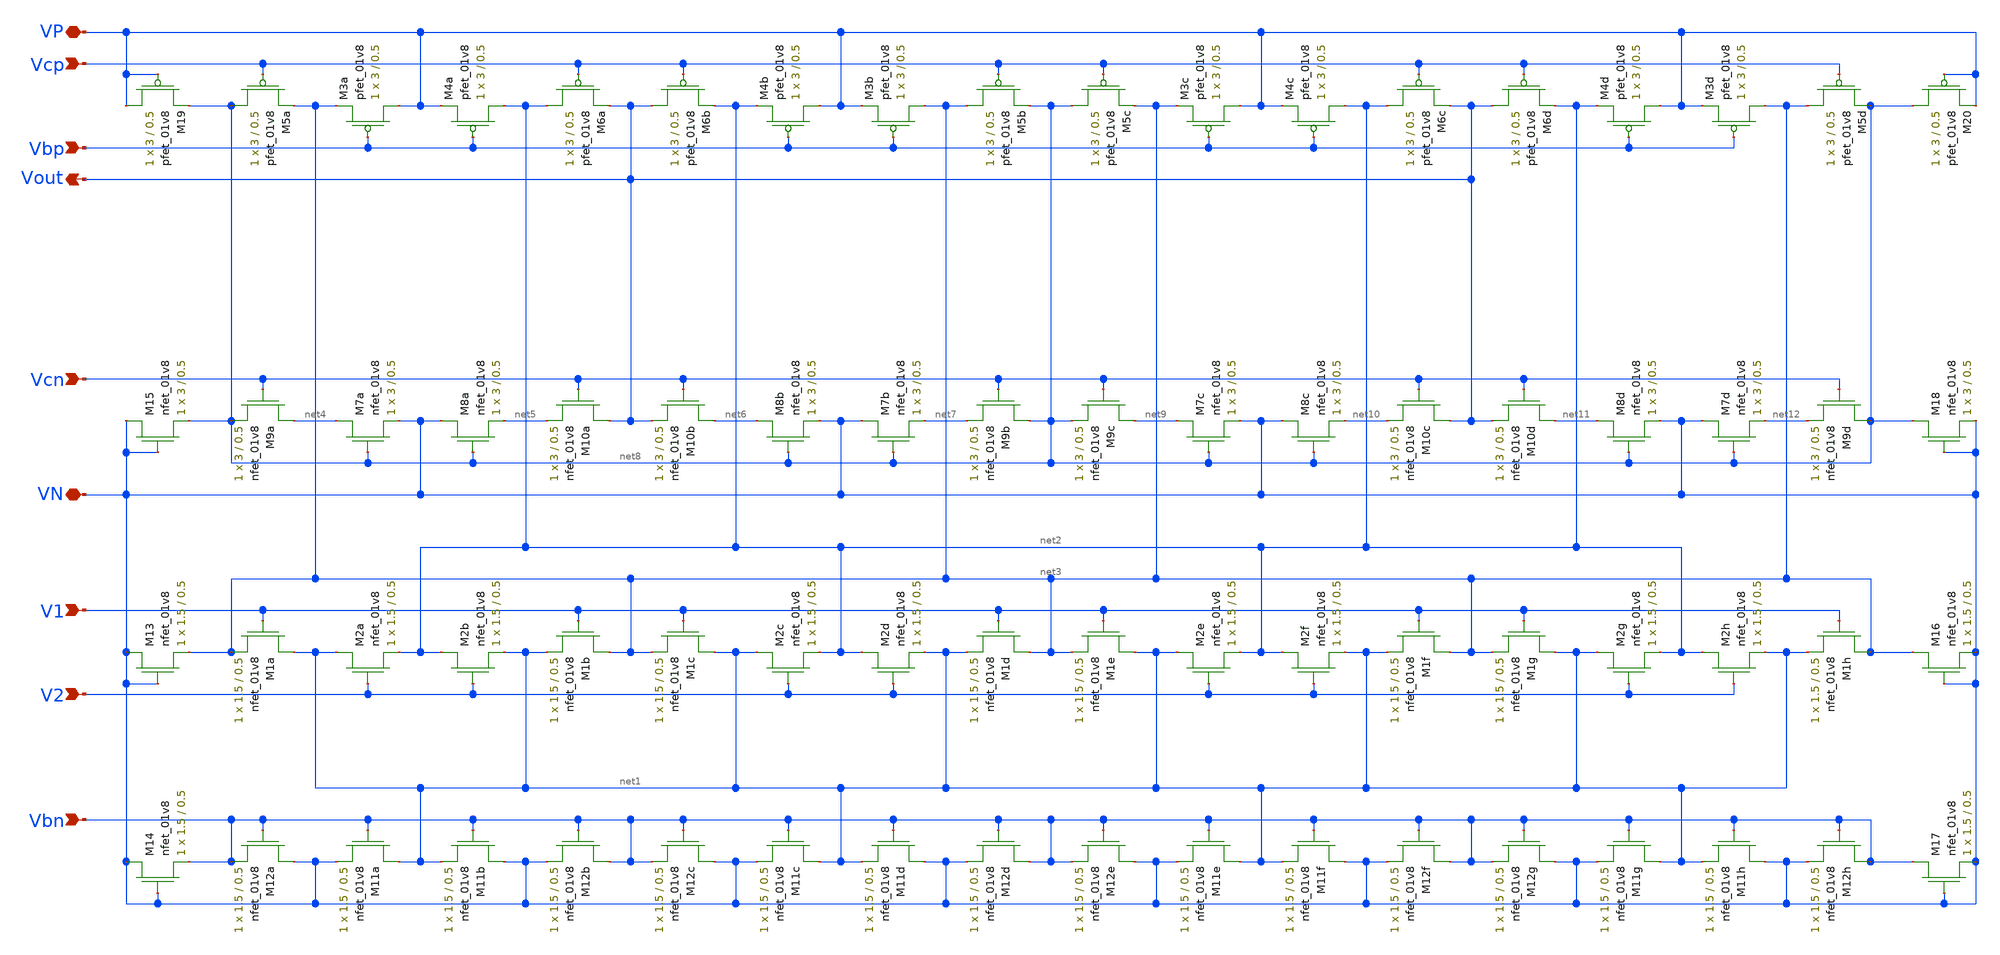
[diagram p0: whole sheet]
** sch_path: fc_diffamp_lds.sch
**.subckt fc_diffamp_lds V1 V2 Vout VN VP Vcp Vbp Vcn Vbn
*.ipin V1
*.ipin V2
*.opin Vout
*.iopin VN
*.iopin VP
*.ipin Vcp
*.ipin Vbp
*.ipin Vcn
*.ipin Vbn
XM1a net1 V1 net3 GND sky130_fd_pr__nfet_01v8 L=0.5 W=1.5 nf=1 ad='int((nf+1)/2) * W/nf * 0.29' as='int((nf+2)/2) * W/nf * 0.29'
+ pd='2*int((nf+1)/2) * (W/nf + 0.29)' ps='2*int((nf+2)/2) * (W/nf + 0.29)' nrd='0.29 / W' nrs='0.29 / W'
+ sa=0 sb=0 sd=0 mult=1 m=1
XM2a net1 V2 net2 GND sky130_fd_pr__nfet_01v8 L=0.5 W=1.5 nf=1 ad='int((nf+1)/2) * W/nf * 0.29' as='int((nf+2)/2) * W/nf * 0.29'
+ pd='2*int((nf+1)/2) * (W/nf + 0.29)' ps='2*int((nf+2)/2) * (W/nf + 0.29)' nrd='0.29 / W' nrs='0.29 / W'
+ sa=0 sb=0 sd=0 mult=1 m=1
XM2b net2 V2 net1 GND sky130_fd_pr__nfet_01v8 L=0.5 W=1.5 nf=1 ad='int((nf+1)/2) * W/nf * 0.29' as='int((nf+2)/2) * W/nf * 0.29'
+ pd='2*int((nf+1)/2) * (W/nf + 0.29)' ps='2*int((nf+2)/2) * (W/nf + 0.29)' nrd='0.29 / W' nrs='0.29 / W'
+ sa=0 sb=0 sd=0 mult=1 m=1
XM1b net3 V1 net1 GND sky130_fd_pr__nfet_01v8 L=0.5 W=1.5 nf=1 ad='int((nf+1)/2) * W/nf * 0.29' as='int((nf+2)/2) * W/nf * 0.29'
+ pd='2*int((nf+1)/2) * (W/nf + 0.29)' ps='2*int((nf+2)/2) * (W/nf + 0.29)' nrd='0.29 / W' nrs='0.29 / W'
+ sa=0 sb=0 sd=0 mult=1 m=1
XM1c net1 V1 net3 GND sky130_fd_pr__nfet_01v8 L=0.5 W=1.5 nf=1 ad='int((nf+1)/2) * W/nf * 0.29' as='int((nf+2)/2) * W/nf * 0.29'
+ pd='2*int((nf+1)/2) * (W/nf + 0.29)' ps='2*int((nf+2)/2) * (W/nf + 0.29)' nrd='0.29 / W' nrs='0.29 / W'
+ sa=0 sb=0 sd=0 mult=1 m=1
XM2c net1 V2 net2 GND sky130_fd_pr__nfet_01v8 L=0.5 W=1.5 nf=1 ad='int((nf+1)/2) * W/nf * 0.29' as='int((nf+2)/2) * W/nf * 0.29'
+ pd='2*int((nf+1)/2) * (W/nf + 0.29)' ps='2*int((nf+2)/2) * (W/nf + 0.29)' nrd='0.29 / W' nrs='0.29 / W'
+ sa=0 sb=0 sd=0 mult=1 m=1
XM2d net2 V2 net1 GND sky130_fd_pr__nfet_01v8 L=0.5 W=1.5 nf=1 ad='int((nf+1)/2) * W/nf * 0.29' as='int((nf+2)/2) * W/nf * 0.29'
+ pd='2*int((nf+1)/2) * (W/nf + 0.29)' ps='2*int((nf+2)/2) * (W/nf + 0.29)' nrd='0.29 / W' nrs='0.29 / W'
+ sa=0 sb=0 sd=0 mult=1 m=1
XM1d net3 V1 net1 GND sky130_fd_pr__nfet_01v8 L=0.5 W=1.5 nf=1 ad='int((nf+1)/2) * W/nf * 0.29' as='int((nf+2)/2) * W/nf * 0.29'
+ pd='2*int((nf+1)/2) * (W/nf + 0.29)' ps='2*int((nf+2)/2) * (W/nf + 0.29)' nrd='0.29 / W' nrs='0.29 / W'
+ sa=0 sb=0 sd=0 mult=1 m=1
XM11a net1 Vbn VN GND sky130_fd_pr__nfet_01v8 L=0.5 W=1.5 nf=1 ad='int((nf+1)/2) * W/nf * 0.29' as='int((nf+2)/2) * W/nf * 0.29'
+ pd='2*int((nf+1)/2) * (W/nf + 0.29)' ps='2*int((nf+2)/2) * (W/nf + 0.29)' nrd='0.29 / W' nrs='0.29 / W'
+ sa=0 sb=0 sd=0 mult=1 m=1
XM12a VN Vbn Vbn GND sky130_fd_pr__nfet_01v8 L=0.5 W=1.5 nf=1 ad='int((nf+1)/2) * W/nf * 0.29' as='int((nf+2)/2) * W/nf * 0.29'
+ pd='2*int((nf+1)/2) * (W/nf + 0.29)' ps='2*int((nf+2)/2) * (W/nf + 0.29)' nrd='0.29 / W' nrs='0.29 / W'
+ sa=0 sb=0 sd=0 mult=1 m=1
XM12b Vbn Vbn VN GND sky130_fd_pr__nfet_01v8 L=0.5 W=1.5 nf=1 ad='int((nf+1)/2) * W/nf * 0.29' as='int((nf+2)/2) * W/nf * 0.29'
+ pd='2*int((nf+1)/2) * (W/nf + 0.29)' ps='2*int((nf+2)/2) * (W/nf + 0.29)' nrd='0.29 / W' nrs='0.29 / W'
+ sa=0 sb=0 sd=0 mult=1 m=1
XM11b VN Vbn net1 GND sky130_fd_pr__nfet_01v8 L=0.5 W=1.5 nf=1 ad='int((nf+1)/2) * W/nf * 0.29' as='int((nf+2)/2) * W/nf * 0.29'
+ pd='2*int((nf+1)/2) * (W/nf + 0.29)' ps='2*int((nf+2)/2) * (W/nf + 0.29)' nrd='0.29 / W' nrs='0.29 / W'
+ sa=0 sb=0 sd=0 mult=1 m=1
XM11c net1 Vbn VN GND sky130_fd_pr__nfet_01v8 L=0.5 W=1.5 nf=1 ad='int((nf+1)/2) * W/nf * 0.29' as='int((nf+2)/2) * W/nf * 0.29'
+ pd='2*int((nf+1)/2) * (W/nf + 0.29)' ps='2*int((nf+2)/2) * (W/nf + 0.29)' nrd='0.29 / W' nrs='0.29 / W'
+ sa=0 sb=0 sd=0 mult=1 m=1
XM12c VN Vbn Vbn GND sky130_fd_pr__nfet_01v8 L=0.5 W=1.5 nf=1 ad='int((nf+1)/2) * W/nf * 0.29' as='int((nf+2)/2) * W/nf * 0.29'
+ pd='2*int((nf+1)/2) * (W/nf + 0.29)' ps='2*int((nf+2)/2) * (W/nf + 0.29)' nrd='0.29 / W' nrs='0.29 / W'
+ sa=0 sb=0 sd=0 mult=1 m=1
XM12d Vbn Vbn VN GND sky130_fd_pr__nfet_01v8 L=0.5 W=1.5 nf=1 ad='int((nf+1)/2) * W/nf * 0.29' as='int((nf+2)/2) * W/nf * 0.29'
+ pd='2*int((nf+1)/2) * (W/nf + 0.29)' ps='2*int((nf+2)/2) * (W/nf + 0.29)' nrd='0.29 / W' nrs='0.29 / W'
+ sa=0 sb=0 sd=0 mult=1 m=1
XM11d VN Vbn net1 GND sky130_fd_pr__nfet_01v8 L=0.5 W=1.5 nf=1 ad='int((nf+1)/2) * W/nf * 0.29' as='int((nf+2)/2) * W/nf * 0.29'
+ pd='2*int((nf+1)/2) * (W/nf + 0.29)' ps='2*int((nf+2)/2) * (W/nf + 0.29)' nrd='0.29 / W' nrs='0.29 / W'
+ sa=0 sb=0 sd=0 mult=1 m=1
XM9a net4 Vcn net8 GND sky130_fd_pr__nfet_01v8 L=0.5 W=3 nf=1 ad='int((nf+1)/2) * W/nf * 0.29' as='int((nf+2)/2) * W/nf * 0.29'
+ pd='2*int((nf+1)/2) * (W/nf + 0.29)' ps='2*int((nf+2)/2) * (W/nf + 0.29)' nrd='0.29 / W' nrs='0.29 / W'
+ sa=0 sb=0 sd=0 mult=1 m=1
XM7a net4 net8 VN GND sky130_fd_pr__nfet_01v8 L=0.5 W=3 nf=1 ad='int((nf+1)/2) * W/nf * 0.29' as='int((nf+2)/2) * W/nf * 0.29'
+ pd='2*int((nf+1)/2) * (W/nf + 0.29)' ps='2*int((nf+2)/2) * (W/nf + 0.29)' nrd='0.29 / W' nrs='0.29 / W'
+ sa=0 sb=0 sd=0 mult=1 m=1
XM8a VN net8 net5 GND sky130_fd_pr__nfet_01v8 L=0.5 W=3 nf=1 ad='int((nf+1)/2) * W/nf * 0.29' as='int((nf+2)/2) * W/nf * 0.29'
+ pd='2*int((nf+1)/2) * (W/nf + 0.29)' ps='2*int((nf+2)/2) * (W/nf + 0.29)' nrd='0.29 / W' nrs='0.29 / W'
+ sa=0 sb=0 sd=0 mult=1 m=1
XM10a Vout Vcn net5 GND sky130_fd_pr__nfet_01v8 L=0.5 W=3 nf=1 ad='int((nf+1)/2) * W/nf * 0.29' as='int((nf+2)/2) * W/nf * 0.29'
+ pd='2*int((nf+1)/2) * (W/nf + 0.29)' ps='2*int((nf+2)/2) * (W/nf + 0.29)' nrd='0.29 / W' nrs='0.29 / W'
+ sa=0 sb=0 sd=0 mult=1 m=1
XM10b net6 Vcn Vout GND sky130_fd_pr__nfet_01v8 L=0.5 W=3 nf=1 ad='int((nf+1)/2) * W/nf * 0.29' as='int((nf+2)/2) * W/nf * 0.29'
+ pd='2*int((nf+1)/2) * (W/nf + 0.29)' ps='2*int((nf+2)/2) * (W/nf + 0.29)' nrd='0.29 / W' nrs='0.29 / W'
+ sa=0 sb=0 sd=0 mult=1 m=1
XM9b net8 Vcn net7 GND sky130_fd_pr__nfet_01v8 L=0.5 W=3 nf=1 ad='int((nf+1)/2) * W/nf * 0.29' as='int((nf+2)/2) * W/nf * 0.29'
+ pd='2*int((nf+1)/2) * (W/nf + 0.29)' ps='2*int((nf+2)/2) * (W/nf + 0.29)' nrd='0.29 / W' nrs='0.29 / W'
+ sa=0 sb=0 sd=0 mult=1 m=1
XM7b VN net8 net7 GND sky130_fd_pr__nfet_01v8 L=0.5 W=3 nf=1 ad='int((nf+1)/2) * W/nf * 0.29' as='int((nf+2)/2) * W/nf * 0.29'
+ pd='2*int((nf+1)/2) * (W/nf + 0.29)' ps='2*int((nf+2)/2) * (W/nf + 0.29)' nrd='0.29 / W' nrs='0.29 / W'
+ sa=0 sb=0 sd=0 mult=1 m=1
XM8b net6 net8 VN GND sky130_fd_pr__nfet_01v8 L=0.5 W=3 nf=1 ad='int((nf+1)/2) * W/nf * 0.29' as='int((nf+2)/2) * W/nf * 0.29'
+ pd='2*int((nf+1)/2) * (W/nf + 0.29)' ps='2*int((nf+2)/2) * (W/nf + 0.29)' nrd='0.29 / W' nrs='0.29 / W'
+ sa=0 sb=0 sd=0 mult=1 m=1
XM9c net9 Vcn net8 GND sky130_fd_pr__nfet_01v8 L=0.5 W=3 nf=1 ad='int((nf+1)/2) * W/nf * 0.29' as='int((nf+2)/2) * W/nf * 0.29'
+ pd='2*int((nf+1)/2) * (W/nf + 0.29)' ps='2*int((nf+2)/2) * (W/nf + 0.29)' nrd='0.29 / W' nrs='0.29 / W'
+ sa=0 sb=0 sd=0 mult=1 m=1
XM7c net9 net8 VN GND sky130_fd_pr__nfet_01v8 L=0.5 W=3 nf=1 ad='int((nf+1)/2) * W/nf * 0.29' as='int((nf+2)/2) * W/nf * 0.29'
+ pd='2*int((nf+1)/2) * (W/nf + 0.29)' ps='2*int((nf+2)/2) * (W/nf + 0.29)' nrd='0.29 / W' nrs='0.29 / W'
+ sa=0 sb=0 sd=0 mult=1 m=1
XM8c VN net8 net10 GND sky130_fd_pr__nfet_01v8 L=0.5 W=3 nf=1 ad='int((nf+1)/2) * W/nf * 0.29' as='int((nf+2)/2) * W/nf * 0.29'
+ pd='2*int((nf+1)/2) * (W/nf + 0.29)' ps='2*int((nf+2)/2) * (W/nf + 0.29)' nrd='0.29 / W' nrs='0.29 / W'
+ sa=0 sb=0 sd=0 mult=1 m=1
XM10c Vout Vcn net10 GND sky130_fd_pr__nfet_01v8 L=0.5 W=3 nf=1 ad='int((nf+1)/2) * W/nf * 0.29' as='int((nf+2)/2) * W/nf * 0.29'
+ pd='2*int((nf+1)/2) * (W/nf + 0.29)' ps='2*int((nf+2)/2) * (W/nf + 0.29)' nrd='0.29 / W' nrs='0.29 / W'
+ sa=0 sb=0 sd=0 mult=1 m=1
XM10d net11 Vcn Vout GND sky130_fd_pr__nfet_01v8 L=0.5 W=3 nf=1 ad='int((nf+1)/2) * W/nf * 0.29' as='int((nf+2)/2) * W/nf * 0.29'
+ pd='2*int((nf+1)/2) * (W/nf + 0.29)' ps='2*int((nf+2)/2) * (W/nf + 0.29)' nrd='0.29 / W' nrs='0.29 / W'
+ sa=0 sb=0 sd=0 mult=1 m=1
XM9d net8 Vcn net12 GND sky130_fd_pr__nfet_01v8 L=0.5 W=3 nf=1 ad='int((nf+1)/2) * W/nf * 0.29' as='int((nf+2)/2) * W/nf * 0.29'
+ pd='2*int((nf+1)/2) * (W/nf + 0.29)' ps='2*int((nf+2)/2) * (W/nf + 0.29)' nrd='0.29 / W' nrs='0.29 / W'
+ sa=0 sb=0 sd=0 mult=1 m=1
XM7d VN net8 net12 GND sky130_fd_pr__nfet_01v8 L=0.5 W=3 nf=1 ad='int((nf+1)/2) * W/nf * 0.29' as='int((nf+2)/2) * W/nf * 0.29'
+ pd='2*int((nf+1)/2) * (W/nf + 0.29)' ps='2*int((nf+2)/2) * (W/nf + 0.29)' nrd='0.29 / W' nrs='0.29 / W'
+ sa=0 sb=0 sd=0 mult=1 m=1
XM8d net11 net8 VN GND sky130_fd_pr__nfet_01v8 L=0.5 W=3 nf=1 ad='int((nf+1)/2) * W/nf * 0.29' as='int((nf+2)/2) * W/nf * 0.29'
+ pd='2*int((nf+1)/2) * (W/nf + 0.29)' ps='2*int((nf+2)/2) * (W/nf + 0.29)' nrd='0.29 / W' nrs='0.29 / W'
+ sa=0 sb=0 sd=0 mult=1 m=1
XM5a net8 Vcp net3 VDD sky130_fd_pr__pfet_01v8 L=0.5 W=3 nf=1 ad='int((nf+1)/2) * W/nf * 0.29' as='int((nf+2)/2) * W/nf * 0.29'
+ pd='2*int((nf+1)/2) * (W/nf + 0.29)' ps='2*int((nf+2)/2) * (W/nf + 0.29)' nrd='0.29 / W' nrs='0.29 / W'
+ sa=0 sb=0 sd=0 mult=1 m=1
XM5b net3 Vcp net8 VDD sky130_fd_pr__pfet_01v8 L=0.5 W=3 nf=1 ad='int((nf+1)/2) * W/nf * 0.29' as='int((nf+2)/2) * W/nf * 0.29'
+ pd='2*int((nf+1)/2) * (W/nf + 0.29)' ps='2*int((nf+2)/2) * (W/nf + 0.29)' nrd='0.29 / W' nrs='0.29 / W'
+ sa=0 sb=0 sd=0 mult=1 m=1
XM5c net8 Vcp net3 VDD sky130_fd_pr__pfet_01v8 L=0.5 W=3 nf=1 ad='int((nf+1)/2) * W/nf * 0.29' as='int((nf+2)/2) * W/nf * 0.29'
+ pd='2*int((nf+1)/2) * (W/nf + 0.29)' ps='2*int((nf+2)/2) * (W/nf + 0.29)' nrd='0.29 / W' nrs='0.29 / W'
+ sa=0 sb=0 sd=0 mult=1 m=1
XM5d net3 Vcp net8 VDD sky130_fd_pr__pfet_01v8 L=0.5 W=3 nf=1 ad='int((nf+1)/2) * W/nf * 0.29' as='int((nf+2)/2) * W/nf * 0.29'
+ pd='2*int((nf+1)/2) * (W/nf + 0.29)' ps='2*int((nf+2)/2) * (W/nf + 0.29)' nrd='0.29 / W' nrs='0.29 / W'
+ sa=0 sb=0 sd=0 mult=1 m=1
XM6a net2 Vcp Vout VDD sky130_fd_pr__pfet_01v8 L=0.5 W=3 nf=1 ad='int((nf+1)/2) * W/nf * 0.29' as='int((nf+2)/2) * W/nf * 0.29'
+ pd='2*int((nf+1)/2) * (W/nf + 0.29)' ps='2*int((nf+2)/2) * (W/nf + 0.29)' nrd='0.29 / W' nrs='0.29 / W'
+ sa=0 sb=0 sd=0 mult=1 m=1
XM6b Vout Vcp net2 VDD sky130_fd_pr__pfet_01v8 L=0.5 W=3 nf=1 ad='int((nf+1)/2) * W/nf * 0.29' as='int((nf+2)/2) * W/nf * 0.29'
+ pd='2*int((nf+1)/2) * (W/nf + 0.29)' ps='2*int((nf+2)/2) * (W/nf + 0.29)' nrd='0.29 / W' nrs='0.29 / W'
+ sa=0 sb=0 sd=0 mult=1 m=1
XM6c net2 Vcp Vout VDD sky130_fd_pr__pfet_01v8 L=0.5 W=3 nf=1 ad='int((nf+1)/2) * W/nf * 0.29' as='int((nf+2)/2) * W/nf * 0.29'
+ pd='2*int((nf+1)/2) * (W/nf + 0.29)' ps='2*int((nf+2)/2) * (W/nf + 0.29)' nrd='0.29 / W' nrs='0.29 / W'
+ sa=0 sb=0 sd=0 mult=1 m=1
XM6d Vout Vcp net2 VDD sky130_fd_pr__pfet_01v8 L=0.5 W=3 nf=1 ad='int((nf+1)/2) * W/nf * 0.29' as='int((nf+2)/2) * W/nf * 0.29'
+ pd='2*int((nf+1)/2) * (W/nf + 0.29)' ps='2*int((nf+2)/2) * (W/nf + 0.29)' nrd='0.29 / W' nrs='0.29 / W'
+ sa=0 sb=0 sd=0 mult=1 m=1
XM3a VP Vbp net3 VDD sky130_fd_pr__pfet_01v8 L=0.5 W=3 nf=1 ad='int((nf+1)/2) * W/nf * 0.29' as='int((nf+2)/2) * W/nf * 0.29'
+ pd='2*int((nf+1)/2) * (W/nf + 0.29)' ps='2*int((nf+2)/2) * (W/nf + 0.29)' nrd='0.29 / W' nrs='0.29 / W'
+ sa=0 sb=0 sd=0 mult=1 m=1
XM3b net3 Vbp VP VDD sky130_fd_pr__pfet_01v8 L=0.5 W=3 nf=1 ad='int((nf+1)/2) * W/nf * 0.29' as='int((nf+2)/2) * W/nf * 0.29'
+ pd='2*int((nf+1)/2) * (W/nf + 0.29)' ps='2*int((nf+2)/2) * (W/nf + 0.29)' nrd='0.29 / W' nrs='0.29 / W'
+ sa=0 sb=0 sd=0 mult=1 m=1
XM3c VP Vbp net3 VDD sky130_fd_pr__pfet_01v8 L=0.5 W=3 nf=1 ad='int((nf+1)/2) * W/nf * 0.29' as='int((nf+2)/2) * W/nf * 0.29'
+ pd='2*int((nf+1)/2) * (W/nf + 0.29)' ps='2*int((nf+2)/2) * (W/nf + 0.29)' nrd='0.29 / W' nrs='0.29 / W'
+ sa=0 sb=0 sd=0 mult=1 m=1
XM3d net3 Vbp VP VDD sky130_fd_pr__pfet_01v8 L=0.5 W=3 nf=1 ad='int((nf+1)/2) * W/nf * 0.29' as='int((nf+2)/2) * W/nf * 0.29'
+ pd='2*int((nf+1)/2) * (W/nf + 0.29)' ps='2*int((nf+2)/2) * (W/nf + 0.29)' nrd='0.29 / W' nrs='0.29 / W'
+ sa=0 sb=0 sd=0 mult=1 m=1
XM4a net2 Vbp VP VDD sky130_fd_pr__pfet_01v8 L=0.5 W=3 nf=1 ad='int((nf+1)/2) * W/nf * 0.29' as='int((nf+2)/2) * W/nf * 0.29'
+ pd='2*int((nf+1)/2) * (W/nf + 0.29)' ps='2*int((nf+2)/2) * (W/nf + 0.29)' nrd='0.29 / W' nrs='0.29 / W'
+ sa=0 sb=0 sd=0 mult=1 m=1
XM4b VP Vbp net2 VDD sky130_fd_pr__pfet_01v8 L=0.5 W=3 nf=1 ad='int((nf+1)/2) * W/nf * 0.29' as='int((nf+2)/2) * W/nf * 0.29'
+ pd='2*int((nf+1)/2) * (W/nf + 0.29)' ps='2*int((nf+2)/2) * (W/nf + 0.29)' nrd='0.29 / W' nrs='0.29 / W'
+ sa=0 sb=0 sd=0 mult=1 m=1
XM4c net2 Vbp VP VDD sky130_fd_pr__pfet_01v8 L=0.5 W=3 nf=1 ad='int((nf+1)/2) * W/nf * 0.29' as='int((nf+2)/2) * W/nf * 0.29'
+ pd='2*int((nf+1)/2) * (W/nf + 0.29)' ps='2*int((nf+2)/2) * (W/nf + 0.29)' nrd='0.29 / W' nrs='0.29 / W'
+ sa=0 sb=0 sd=0 mult=1 m=1
XM4d VP Vbp net2 VDD sky130_fd_pr__pfet_01v8 L=0.5 W=3 nf=1 ad='int((nf+1)/2) * W/nf * 0.29' as='int((nf+2)/2) * W/nf * 0.29'
+ pd='2*int((nf+1)/2) * (W/nf + 0.29)' ps='2*int((nf+2)/2) * (W/nf + 0.29)' nrd='0.29 / W' nrs='0.29 / W'
+ sa=0 sb=0 sd=0 mult=1 m=1
XM13 VN VN net3 GND sky130_fd_pr__nfet_01v8 L=0.5 W=1.5 nf=1 ad='int((nf+1)/2) * W/nf * 0.29' as='int((nf+2)/2) * W/nf * 0.29'
+ pd='2*int((nf+1)/2) * (W/nf + 0.29)' ps='2*int((nf+2)/2) * (W/nf + 0.29)' nrd='0.29 / W' nrs='0.29 / W'
+ sa=0 sb=0 sd=0 mult=1 m=1
XM15 VN VN net8 GND sky130_fd_pr__nfet_01v8 L=0.5 W=3 nf=1 ad='int((nf+1)/2) * W/nf * 0.29' as='int((nf+2)/2) * W/nf * 0.29'
+ pd='2*int((nf+1)/2) * (W/nf + 0.29)' ps='2*int((nf+2)/2) * (W/nf + 0.29)' nrd='0.29 / W' nrs='0.29 / W'
+ sa=0 sb=0 sd=0 mult=1 m=1
XM17 Vbn VN VN GND sky130_fd_pr__nfet_01v8 L=0.5 W=1.5 nf=1 ad='int((nf+1)/2) * W/nf * 0.29' as='int((nf+2)/2) * W/nf * 0.29'
+ pd='2*int((nf+1)/2) * (W/nf + 0.29)' ps='2*int((nf+2)/2) * (W/nf + 0.29)' nrd='0.29 / W' nrs='0.29 / W'
+ sa=0 sb=0 sd=0 mult=1 m=1
XM18 net8 VN VN GND sky130_fd_pr__nfet_01v8 L=0.5 W=3 nf=1 ad='int((nf+1)/2) * W/nf * 0.29' as='int((nf+2)/2) * W/nf * 0.29'
+ pd='2*int((nf+1)/2) * (W/nf + 0.29)' ps='2*int((nf+2)/2) * (W/nf + 0.29)' nrd='0.29 / W' nrs='0.29 / W'
+ sa=0 sb=0 sd=0 mult=1 m=1
XM19 VP VP net8 VDD sky130_fd_pr__pfet_01v8 L=0.5 W=3 nf=1 ad='int((nf+1)/2) * W/nf * 0.29' as='int((nf+2)/2) * W/nf * 0.29'
+ pd='2*int((nf+1)/2) * (W/nf + 0.29)' ps='2*int((nf+2)/2) * (W/nf + 0.29)' nrd='0.29 / W' nrs='0.29 / W'
+ sa=0 sb=0 sd=0 mult=1 m=1
XM20 net8 VP VP VDD sky130_fd_pr__pfet_01v8 L=0.5 W=3 nf=1 ad='int((nf+1)/2) * W/nf * 0.29' as='int((nf+2)/2) * W/nf * 0.29'
+ pd='2*int((nf+1)/2) * (W/nf + 0.29)' ps='2*int((nf+2)/2) * (W/nf + 0.29)' nrd='0.29 / W' nrs='0.29 / W'
+ sa=0 sb=0 sd=0 mult=1 m=1
XM1e net1 V1 net3 GND sky130_fd_pr__nfet_01v8 L=0.5 W=1.5 nf=1 ad='int((nf+1)/2) * W/nf * 0.29' as='int((nf+2)/2) * W/nf * 0.29'
+ pd='2*int((nf+1)/2) * (W/nf + 0.29)' ps='2*int((nf+2)/2) * (W/nf + 0.29)' nrd='0.29 / W' nrs='0.29 / W'
+ sa=0 sb=0 sd=0 mult=1 m=1
XM2e net1 V2 net2 GND sky130_fd_pr__nfet_01v8 L=0.5 W=1.5 nf=1 ad='int((nf+1)/2) * W/nf * 0.29' as='int((nf+2)/2) * W/nf * 0.29'
+ pd='2*int((nf+1)/2) * (W/nf + 0.29)' ps='2*int((nf+2)/2) * (W/nf + 0.29)' nrd='0.29 / W' nrs='0.29 / W'
+ sa=0 sb=0 sd=0 mult=1 m=1
XM2f net2 V2 net1 GND sky130_fd_pr__nfet_01v8 L=0.5 W=1.5 nf=1 ad='int((nf+1)/2) * W/nf * 0.29' as='int((nf+2)/2) * W/nf * 0.29'
+ pd='2*int((nf+1)/2) * (W/nf + 0.29)' ps='2*int((nf+2)/2) * (W/nf + 0.29)' nrd='0.29 / W' nrs='0.29 / W'
+ sa=0 sb=0 sd=0 mult=1 m=1
XM1f net3 V1 net1 GND sky130_fd_pr__nfet_01v8 L=0.5 W=1.5 nf=1 ad='int((nf+1)/2) * W/nf * 0.29' as='int((nf+2)/2) * W/nf * 0.29'
+ pd='2*int((nf+1)/2) * (W/nf + 0.29)' ps='2*int((nf+2)/2) * (W/nf + 0.29)' nrd='0.29 / W' nrs='0.29 / W'
+ sa=0 sb=0 sd=0 mult=1 m=1
XM1g net1 V1 net3 GND sky130_fd_pr__nfet_01v8 L=0.5 W=1.5 nf=1 ad='int((nf+1)/2) * W/nf * 0.29' as='int((nf+2)/2) * W/nf * 0.29'
+ pd='2*int((nf+1)/2) * (W/nf + 0.29)' ps='2*int((nf+2)/2) * (W/nf + 0.29)' nrd='0.29 / W' nrs='0.29 / W'
+ sa=0 sb=0 sd=0 mult=1 m=1
XM2g net1 V2 net2 GND sky130_fd_pr__nfet_01v8 L=0.5 W=1.5 nf=1 ad='int((nf+1)/2) * W/nf * 0.29' as='int((nf+2)/2) * W/nf * 0.29'
+ pd='2*int((nf+1)/2) * (W/nf + 0.29)' ps='2*int((nf+2)/2) * (W/nf + 0.29)' nrd='0.29 / W' nrs='0.29 / W'
+ sa=0 sb=0 sd=0 mult=1 m=1
XM2h net2 V2 net1 GND sky130_fd_pr__nfet_01v8 L=0.5 W=1.5 nf=1 ad='int((nf+1)/2) * W/nf * 0.29' as='int((nf+2)/2) * W/nf * 0.29'
+ pd='2*int((nf+1)/2) * (W/nf + 0.29)' ps='2*int((nf+2)/2) * (W/nf + 0.29)' nrd='0.29 / W' nrs='0.29 / W'
+ sa=0 sb=0 sd=0 mult=1 m=1
XM1h net3 V1 net1 GND sky130_fd_pr__nfet_01v8 L=0.5 W=1.5 nf=1 ad='int((nf+1)/2) * W/nf * 0.29' as='int((nf+2)/2) * W/nf * 0.29'
+ pd='2*int((nf+1)/2) * (W/nf + 0.29)' ps='2*int((nf+2)/2) * (W/nf + 0.29)' nrd='0.29 / W' nrs='0.29 / W'
+ sa=0 sb=0 sd=0 mult=1 m=1
XM16 net3 VN VN GND sky130_fd_pr__nfet_01v8 L=0.5 W=1.5 nf=1 ad='int((nf+1)/2) * W/nf * 0.29' as='int((nf+2)/2) * W/nf * 0.29'
+ pd='2*int((nf+1)/2) * (W/nf + 0.29)' ps='2*int((nf+2)/2) * (W/nf + 0.29)' nrd='0.29 / W' nrs='0.29 / W'
+ sa=0 sb=0 sd=0 mult=1 m=1
XM11e net1 Vbn VN GND sky130_fd_pr__nfet_01v8 L=0.5 W=1.5 nf=1 ad='int((nf+1)/2) * W/nf * 0.29' as='int((nf+2)/2) * W/nf * 0.29'
+ pd='2*int((nf+1)/2) * (W/nf + 0.29)' ps='2*int((nf+2)/2) * (W/nf + 0.29)' nrd='0.29 / W' nrs='0.29 / W'
+ sa=0 sb=0 sd=0 mult=1 m=1
XM12e VN Vbn Vbn GND sky130_fd_pr__nfet_01v8 L=0.5 W=1.5 nf=1 ad='int((nf+1)/2) * W/nf * 0.29' as='int((nf+2)/2) * W/nf * 0.29'
+ pd='2*int((nf+1)/2) * (W/nf + 0.29)' ps='2*int((nf+2)/2) * (W/nf + 0.29)' nrd='0.29 / W' nrs='0.29 / W'
+ sa=0 sb=0 sd=0 mult=1 m=1
XM12f Vbn Vbn VN GND sky130_fd_pr__nfet_01v8 L=0.5 W=1.5 nf=1 ad='int((nf+1)/2) * W/nf * 0.29' as='int((nf+2)/2) * W/nf * 0.29'
+ pd='2*int((nf+1)/2) * (W/nf + 0.29)' ps='2*int((nf+2)/2) * (W/nf + 0.29)' nrd='0.29 / W' nrs='0.29 / W'
+ sa=0 sb=0 sd=0 mult=1 m=1
XM11f VN Vbn net1 GND sky130_fd_pr__nfet_01v8 L=0.5 W=1.5 nf=1 ad='int((nf+1)/2) * W/nf * 0.29' as='int((nf+2)/2) * W/nf * 0.29'
+ pd='2*int((nf+1)/2) * (W/nf + 0.29)' ps='2*int((nf+2)/2) * (W/nf + 0.29)' nrd='0.29 / W' nrs='0.29 / W'
+ sa=0 sb=0 sd=0 mult=1 m=1
XM11g net1 Vbn VN GND sky130_fd_pr__nfet_01v8 L=0.5 W=1.5 nf=1 ad='int((nf+1)/2) * W/nf * 0.29' as='int((nf+2)/2) * W/nf * 0.29'
+ pd='2*int((nf+1)/2) * (W/nf + 0.29)' ps='2*int((nf+2)/2) * (W/nf + 0.29)' nrd='0.29 / W' nrs='0.29 / W'
+ sa=0 sb=0 sd=0 mult=1 m=1
XM12g VN Vbn Vbn GND sky130_fd_pr__nfet_01v8 L=0.5 W=1.5 nf=1 ad='int((nf+1)/2) * W/nf * 0.29' as='int((nf+2)/2) * W/nf * 0.29'
+ pd='2*int((nf+1)/2) * (W/nf + 0.29)' ps='2*int((nf+2)/2) * (W/nf + 0.29)' nrd='0.29 / W' nrs='0.29 / W'
+ sa=0 sb=0 sd=0 mult=1 m=1
XM12h Vbn Vbn VN GND sky130_fd_pr__nfet_01v8 L=0.5 W=1.5 nf=1 ad='int((nf+1)/2) * W/nf * 0.29' as='int((nf+2)/2) * W/nf * 0.29'
+ pd='2*int((nf+1)/2) * (W/nf + 0.29)' ps='2*int((nf+2)/2) * (W/nf + 0.29)' nrd='0.29 / W' nrs='0.29 / W'
+ sa=0 sb=0 sd=0 mult=1 m=1
XM11h VN Vbn net1 GND sky130_fd_pr__nfet_01v8 L=0.5 W=1.5 nf=1 ad='int((nf+1)/2) * W/nf * 0.29' as='int((nf+2)/2) * W/nf * 0.29'
+ pd='2*int((nf+1)/2) * (W/nf + 0.29)' ps='2*int((nf+2)/2) * (W/nf + 0.29)' nrd='0.29 / W' nrs='0.29 / W'
+ sa=0 sb=0 sd=0 mult=1 m=1
XM14 VN VN Vbn GND sky130_fd_pr__nfet_01v8 L=0.5 W=1.5 nf=1 ad='int((nf+1)/2) * W/nf * 0.29' as='int((nf+2)/2) * W/nf * 0.29'
+ pd='2*int((nf+1)/2) * (W/nf + 0.29)' ps='2*int((nf+2)/2) * (W/nf + 0.29)' nrd='0.29 / W' nrs='0.29 / W'
+ sa=0 sb=0 sd=0 mult=1 m=1
**.ends
.end
